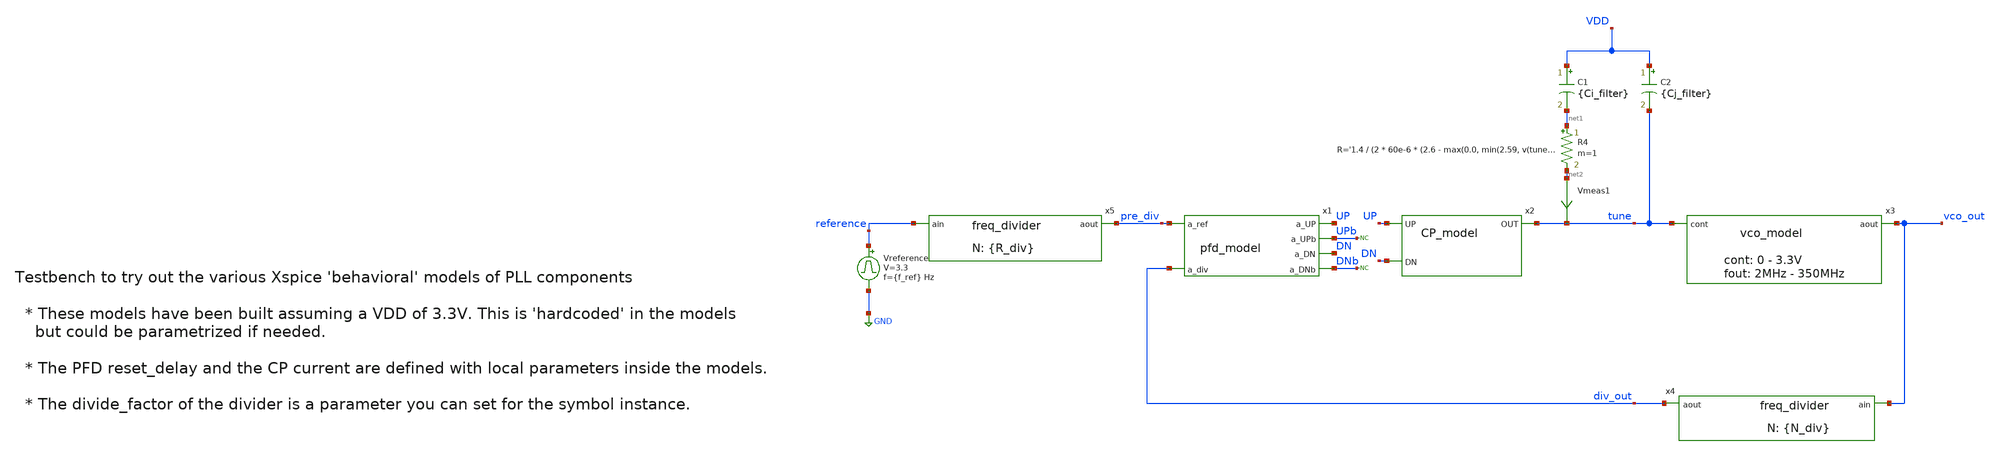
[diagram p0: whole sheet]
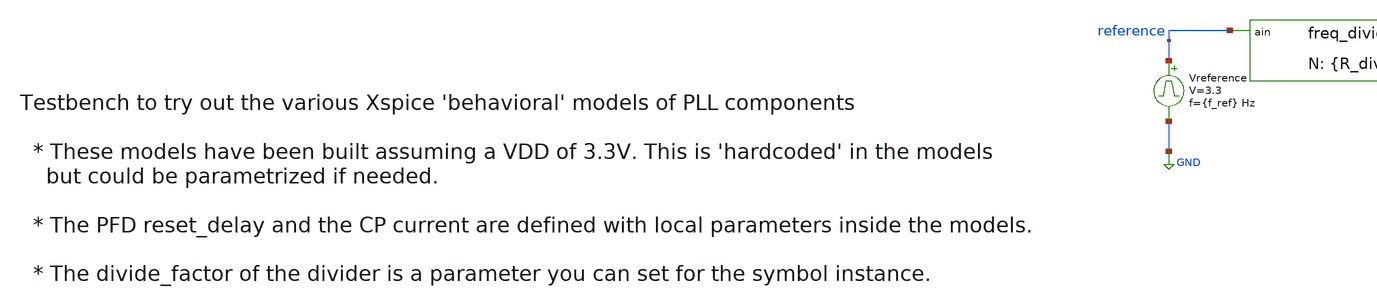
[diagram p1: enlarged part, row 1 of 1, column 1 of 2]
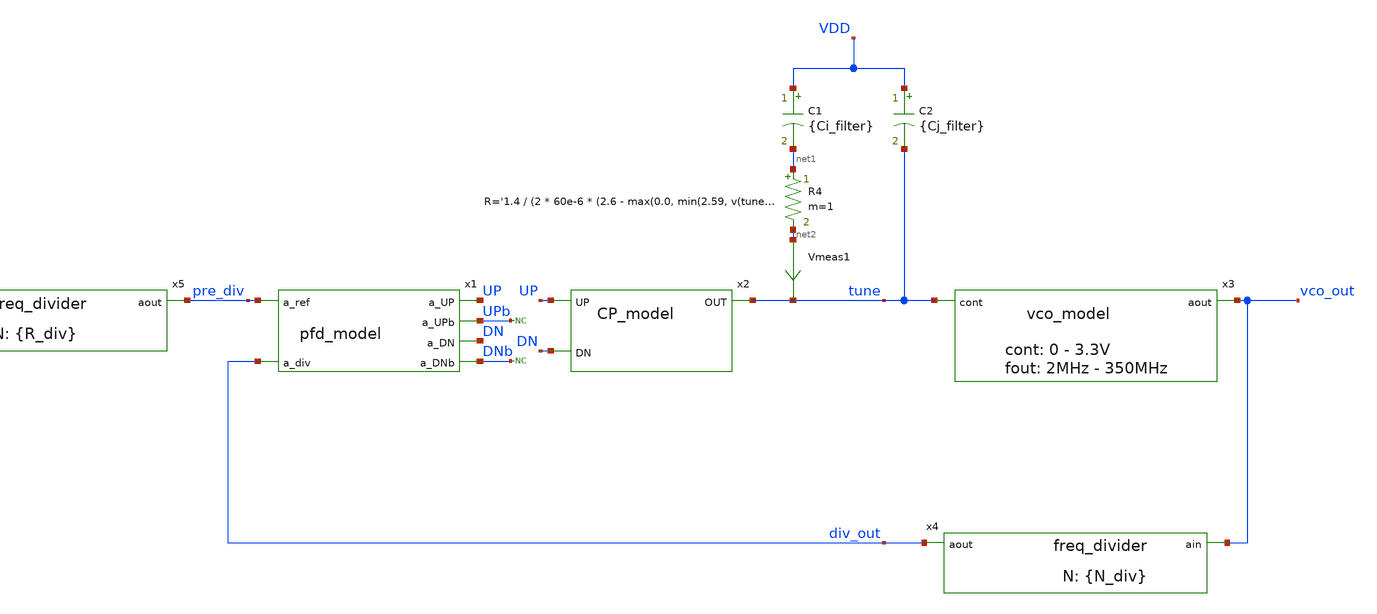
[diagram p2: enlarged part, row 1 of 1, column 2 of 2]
** sch_path: designs/libs/model_pll/tb_PLL_model_phase_noise.sch
**.subckt tb_PLL_model_phase_noise
Vreference reference GND pulse 0 3.3 '0.495/ {f_ref} ' '0.01/{f_ref} ' '0.01/{f_ref} ' '0.49/{f_ref} '
+ '1/{f_ref} '
C1 VDD net1 {Ci_filter} m=1
R4 net1 net2 R='1.4 / (2 * 60e-6 * (2.6 - max(0.0, min(2.59, v(tune)))))' m=1
* noconn DNb
* noconn UPb
C2 VDD tune {Cj_filter} m=1
x1 pre_div UP UPb DN div_out DNb pfd_model
x2 tune UP DN CP_model
x3 vco_out tune vco_model
x4 div_out vco_out freq_divider divide_factor={N_div}
Vmeas1 net2 tune 0
.save i(vmeas1)
x5 pre_div reference freq_divider divide_factor={R_div}
**** begin user architecture code


.control
set wr_singlescale
set wr_vecnames
save all
TRAN 1n 500u 0 100p
remzerovec
*linearize v(vco_out)
write tb_PLL_model_phase_noise.raw
wrdata
+ /foss/designs/synchronos-chipathon-2026/designs/libs/scripts/sim_data/tb_PLL_model_phase_noise.txt tran.all
*fft v(vco_out)
*plot mag(v(vco_out)) xlimit 10k 2G xlog ylog
.endc




.options method=gear
.options reltol=1e-5
VDD VDD 0 3.3
* control is for tests when opening the loop
* see the Vcontrol voltage source
.ic v(tune)=2.6
* reference frequency
.param f_ref = 10MEG
* divider
.param R_div=10
.param N_div=70
* loop filter parameters
.param Ci_filter = 10p
.param Cj_filter = 1p


**** end user architecture code
**.ends

* expanding   symbol:  libs/model_pll/pfd_model.sym # of pins=6
** sym_path: designs/libs/model_pll/pfd_model.sym
** sch_path: designs/libs/model_pll/pfd_model.sch
.subckt pfd_model a_ref a_UP a_UPb a_DN a_div a_DNb
*.ipin a_ref
*.ipin a_div
*.opin a_UP
*.opin a_UPb
*.opin a_DN
*.opin a_DNb
* noconn a_ref
* noconn a_div
* noconn a_UP
* noconn a_UPb
* noconn a_DN
* noconn a_DNb
**** begin user architecture code


* PFD Model using digital Xspice components

* pfd_delay local parameter sets the duration of the overlap (dead-band elimination)
* Reduced from 10ns to 200ps to prevent massive Vctrl ripple
*.param pfd_delay = 200p
.param pfd_delay = 1.5n

** Digital 1 and 0 to drive Flip-Flops
aone 0 d_d1 d_inv
azero d_d1 d_d0 d_inv
.model d_inv d_inverter()

** Flip Flops
ad1 d_d1 d_R d_d0 d_rset d_U d_U_ flop1
ad2 d_d1 d_V d_d0 d_rset d_D d_D_ flop1
.model flop1 d_dff(clk_delay = 1.0e-10 set_delay = 1.0e-10  reset_delay = {pfd_delay} ic = 2 rise_delay
+ = 1.0e-10  fall_delay = 1e-10)

* AND Gate
aa1 [d_U d_D] d_rset and1
.model and1 d_and(rise_delay = 1e-10 fall_delay = 1e-10   input_load = 0.5e-12)

* WINDOW FIX: Widened thresholds to catch fast analog edges safely
aADC [ a_ref a_div ] [ d_R d_V ] adc_buff
.model adc_buff adc_bridge(in_low = 1.2 in_high = 2.1 rise_delay = 10p fall_delay = 10p)

* DAC FIX: Explicitly defined analog rise/fall times to prevent solver crashes
aDAC [ d_U d_U_ d_D d_D_ d_rset d_R d_V d_d1 d_d0 ] [ a_UP a_UPb a_DN a_DNb a_rset a_R a_V a_d1
+ a_d0] dac_buff
.model dac_buff dac_bridge(out_low = 0 out_high = 3.3 t_rise = 500p t_fall = 500p)


**** end user architecture code
.ends


* expanding   symbol:  libs/model_pll/CP_model.sym # of pins=3
** sym_path: designs/libs/model_pll/CP_model.sym
** sch_path: designs/libs/model_pll/CP_model.sch
.subckt CP_model OUT UP DN
*.ipin UP
*.ipin DN
*.opin OUT
**** begin user architecture code


* Bulletproof Charge Pump: Continuous Triode-Region Soft-Clipping
.param param_k = 60e-6

* UP (Sinks to Ground): Smoothly rolls off current as Vctrl drops from 0.1V to 0V
B_Iup OUT 0 I='V(UP) > 1.65 ? (param_k * ((2.6 - max(0.2, min(2.6, V(OUT))))^2 + 0.001)) * max(0, min(1, V(OUT)/0.1)) : 0'

* DN (Sources from VDD): Smoothly rolls off current as Vctrl rises from 3.2V to 3.3V
B_Idn OUT 0 I='V(DN) > 1.65 ? -(param_k * ((2.6 - max(0.2, min(2.6, V(OUT))))^2 + 0.001)) * max(0, min(1, (3.3 - V(OUT))/0.1)) : 0'


**** end user architecture code
* noconn UP
* noconn DN
* noconn OUT
.ends


* expanding   symbol:  libs/model_pll/vco_model.sym # of pins=2
** sym_path: designs/libs/model_pll/vco_model.sym
** sch_path: designs/libs/model_pll/vco_model.sch
.subckt vco_model aout cont
*.ipin cont
*.opin aout
**** begin user architecture code


***** XSPICE analog sine VCO ***************

.param vdd=3.3
.param vthp=0.7
.param vdsat=0.2
.param upper_limit=vdd-vthp-vdsat
.param lower_limit=0.2
asine cont aout analog_sin_osc
.model analog_sin_osc sine(  cntl_array = [ 0.0  3.3 ]   freq_array = [ 400MEG 10k  ]  out_high =
+ 3.3 out_low = 0.0 )


**** end user architecture code
* noconn aout
* noconn cont
.ends


* expanding   symbol:  libs/model_pll/freq_divider.sym # of pins=2
** sym_path: libs/model_pll/freq_divider.sym
** sch_path: libs/model_pll/freq_divider.sch
.subckt freq_divider aout ain  divide_factor=20
*.ipin ain
*.opin aout
* noconn ain
* noconn aout
**** begin user architecture code


* Behavioral Frequency Divider with robust Mixed-Signal Bridges

* Top-level parameter (Defaults to 10 if not passed by symbol)
.param divide_factor = 10

* MATH FIX: Guarantees at least 1 high cycle, targets 50% duty cycle
.param high_cycles = {max(1, floor(divide_factor/2))}

* Xspice digital frequency divider
adiv din dout divider
.model divider d_fdiv(div_factor = {divide_factor}  high_cycles = {high_cycles}  i_count = 0  rise_delay
+ = 10p fall_delay = 10p )

* WINDOW FIX: Widened analog-to-digital thresholds to catch fast sine waves
aADC [ ain ] [ din ] adc_buff
.model adc_buff adc_bridge(in_low = 1.2 in_high = 2.1 rise_delay = 10p fall_delay = 10p)

* Digital-to-analog bridge
aDAC [ dout ] [ aout ] dac_buff
.model dac_buff dac_bridge(out_low = 0 out_high = 3.3 t_rise = 10p t_fall = 10p)


**** end user architecture code
.ends

.GLOBAL GND
.end
